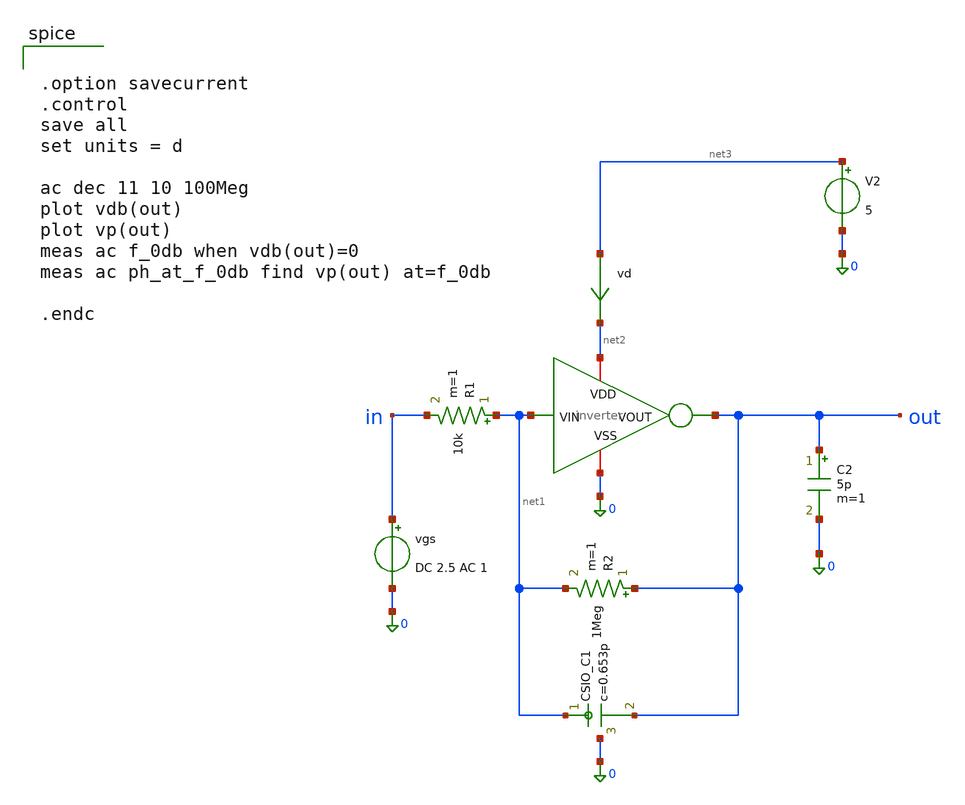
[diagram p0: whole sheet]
** sch_path: member_project/JJY_Receiver/Masahiro/jjy_recv/pre_amp/inverter_sim_ac.sch
**.subckt inverter_sim_ac
vgs in 0 DC 2.5 AC 1
V2 net3 0 5
vd net3 net2 0
.save i(vd)
R2 out net1 1Meg m=1
R1 net1 in 10k m=1
x1 net2 net1 out 0 inverter
XC1 net1 out 0 F_CSIO c=0.653p x=33u y=33u m=1
C2 out 0 5p m=1
**** begin user architecture code
 .include $::LIB/ip62_models


.option savecurrent
.control
save all
set units = d

ac dec 11 10 100Meg
plot vdb(out)
plot vp(out)
meas ac f_0db when vdb(out)=0
meas ac ph_at_f_0db find vp(out) at=f_0db

.endc


**** end user architecture code
**.ends

* expanding   symbol:  inverter.sym # of pins=4
** sym_path: member_project/JJY_Receiver/Masahiro/jjy_recv/pre_amp/inverter.sym
** sch_path: member_project/JJY_Receiver/Masahiro/jjy_recv/pre_amp/inverter.sch
.subckt inverter VDD VIN VOUT VSS
*.ipin VIN
*.opin VOUT
*.iopin VSS
*.iopin VDD
XM1 VOUT VIN VSS VSS NMOS w=6.8u l=10u as=0 ad=0 ps=0 pd=0 nrd=0 nrs=0 m=1
XM2 VOUT VIN VDD VDD PMOS w=20u l=10u as=0 ad=0 ps=0 pd=0 nrd=0 nrs=0 m=1
.ends

.end
